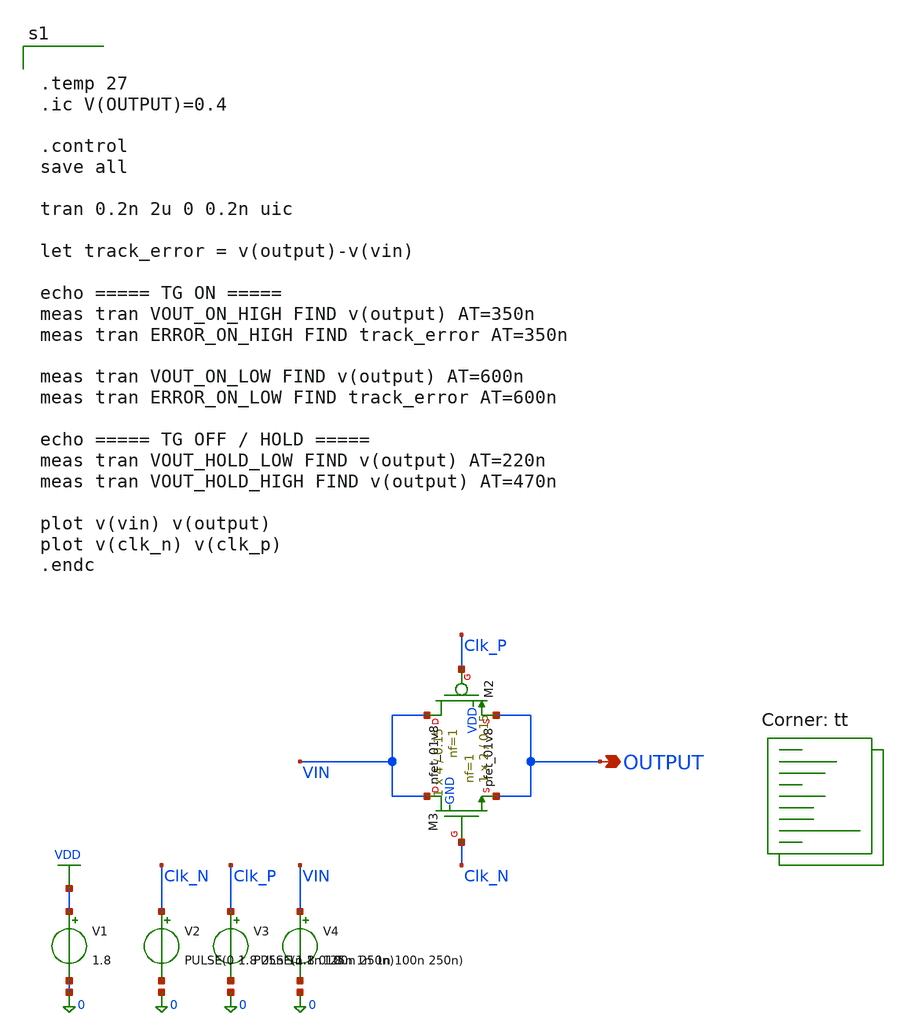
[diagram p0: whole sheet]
** sch_path: blocks/02_CMFB/xschem/TG.sch
**.subckt TG OUTPUT
*.opin OUTPUT
XM2 VIN Clk_P OUTPUT VDD sky130_fd_pr__pfet_01v8 L=0.15 W=4 nf=1 ad='int((1 + 1)/2) * 4 / 1 * 0.29' as='int((1 + 2)/2) * 4 / 1 * 0.29'
+ pd='2*int((1 + 1)/2) * (4 / 1 + 0.29)' ps='2*int((1 + 2)/2) * (4 / 1 + 0.29)' nrd='0.29 / 4 ' nrs='0.29 / 4 '
+ sa=0 sb=0 sd=0 mult=1 m=1
XM3 VIN Clk_N OUTPUT GND sky130_fd_pr__nfet_01v8 L=0.15 W=2 nf=1 ad='int((1 + 1)/2) * 2 / 1 * 0.29' as='int((1 + 2)/2) * 2 / 1 * 0.29'
+ pd='2*int((1 + 1)/2) * (2 / 1 + 0.29)' ps='2*int((1 + 2)/2) * (2 / 1 + 0.29)' nrd='0.29 / 2 ' nrs='0.29 / 2 '
+ sa=0 sb=0 sd=0 mult=1 m=1
V1 VDD 0 1.8
V2 Clk_N net1 PULSE(0 1.8 25n 1n 1n 100n 250n)
V3 Clk_P net2 PULSE(1.8 0 25n 1n 1n 100n 250n)
V4 VIN net3 1.8
**** begin user architecture code


.temp 27
.ic V(OUTPUT)=0.4

.control
save all

tran 0.2n 2u 0 0.2n uic

let track_error = v(output)-v(vin)

echo ===== TG ON =====
meas tran VOUT_ON_HIGH FIND v(output) AT=350n
meas tran ERROR_ON_HIGH FIND track_error AT=350n

meas tran VOUT_ON_LOW FIND v(output) AT=600n
meas tran ERROR_ON_LOW FIND track_error AT=600n

echo ===== TG OFF / HOLD =====
meas tran VOUT_HOLD_LOW FIND v(output) AT=220n
meas tran VOUT_HOLD_HIGH FIND v(output) AT=470n

plot v(vin) v(output)
plot v(clk_n) v(clk_p)
.endc

.lib $::SKYWATER_MODELS/sky130.lib.spice tt
**** end user architecture code
**.ends
.GLOBAL VDD
.end
